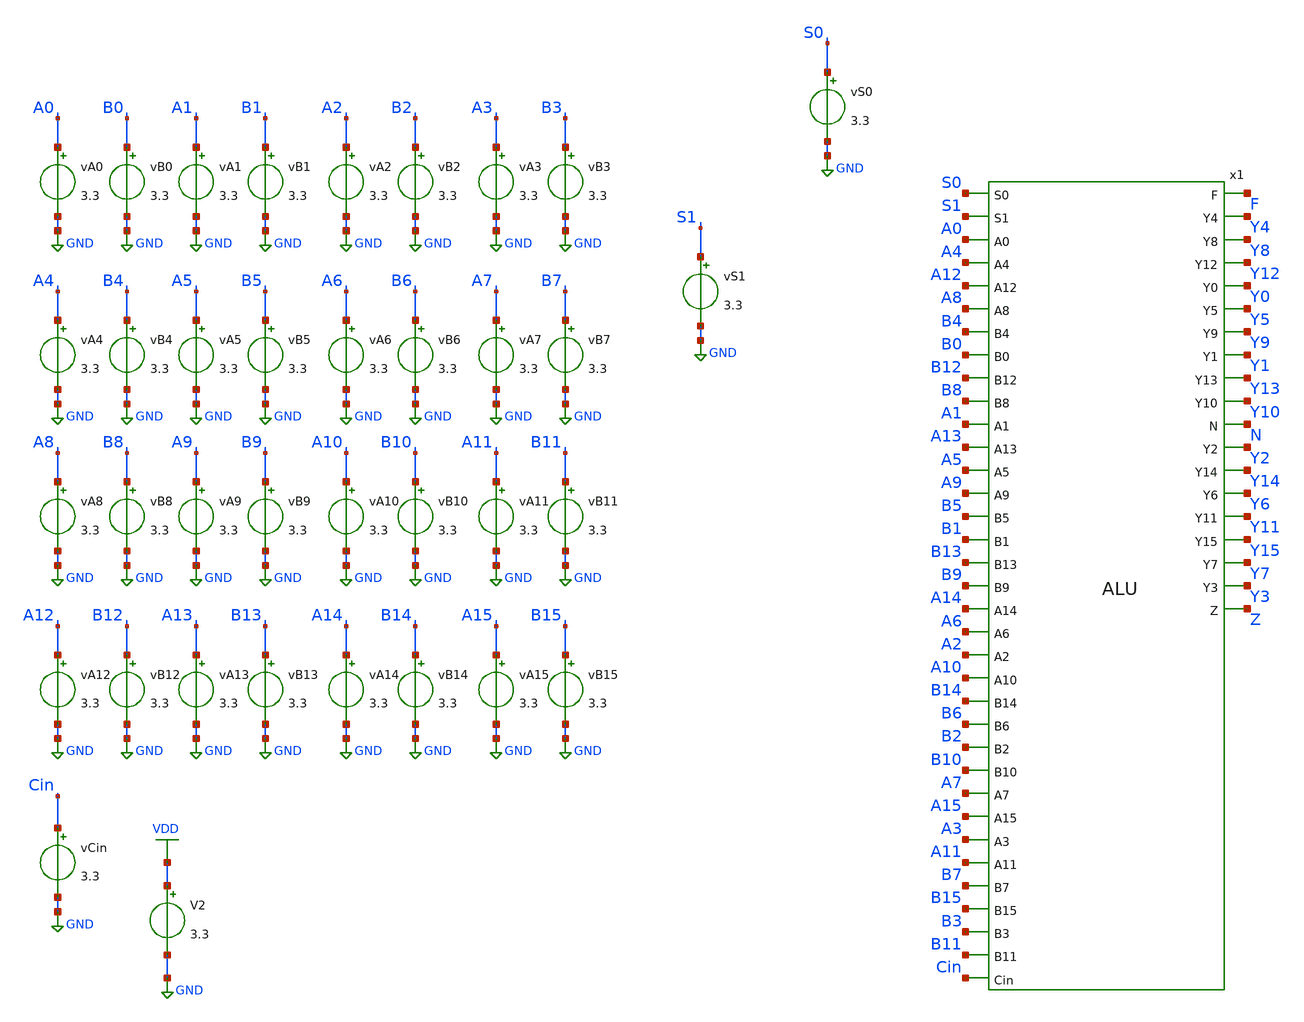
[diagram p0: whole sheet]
** sch_path: tbs/alu_tb_cmpless.sch
**.subckt alu_tb_cmpless
x1 S0 S1 F A0 A4 A12 A8 B4 B0 B12 B8 A1 A13 A5 A9 Y4 Y8 Y12 Y0 B5 B1 B13 B9 Y5 Y9 Y1 Y13 A14 A6 A2
+ A10 Y10 N Y2 Y14 Y6 B14 B6 B2 B10 Y11 Y15 Y7 Y3 A7 A15 A3 A11 B7 B15 B3 B11 Cin Z ALU
vA0 A0 GND 3.3
vB0 B0 GND 3.3
vA1 A1 GND 3.3
vB1 B1 GND 3.3
vA2 A2 GND 3.3
vB2 B2 GND 3.3
vA3 A3 GND 3.3
vB3 B3 GND 3.3
vA4 A4 GND 3.3
vB4 B4 GND 3.3
vA5 A5 GND 3.3
vB5 B5 GND 3.3
vA6 A6 GND 3.3
vB6 B6 GND 3.3
vA7 A7 GND 3.3
vB7 B7 GND 3.3
vA8 A8 GND 3.3
vB8 B8 GND 3.3
vA9 A9 GND 3.3
vB9 B9 GND 3.3
vA10 A10 GND 3.3
vB10 B10 GND 3.3
vA11 A11 GND 3.3
vB11 B11 GND 3.3
vA12 A12 GND 3.3
vB12 B12 GND 3.3
vA13 A13 GND 3.3
vB13 B13 GND 3.3
vA14 A14 GND 3.3
vB14 B14 GND 3.3
vA15 A15 GND 3.3
vB15 B15 GND 3.3
vS0 S0 GND 3.3
vS1 S1 GND 3.3
vCin Cin GND 3.3
V2 VDD GND 3.3
**** begin user architecture code


.control
  let vlow = 0
  let vhigh = 3.3

  * CMP via A + ~B + 1
  alter VS1 = $&vlow
  alter VS0 = $&vlow
  alter VCin = $&vhigh

  * A = 0x0003
  alter VA15 = $&vlow
  alter VA14 = $&vlow
  alter VA13 = $&vlow
  alter VA12 = $&vlow
  alter VA11 = $&vlow
  alter VA10 = $&vlow
  alter VA9  = $&vlow
  alter VA8  = $&vlow
  alter VA7  = $&vlow
  alter VA6  = $&vlow
  alter VA5  = $&vlow
  alter VA4  = $&vlow
  alter VA3  = $&vlow
  alter VA2  = $&vlow
  alter VA1  = $&vhigh
  alter VA0  = $&vhigh

  * B = ~0x0005 = 0xFFFA
  alter VB15 = $&vhigh
  alter VB14 = $&vhigh
  alter VB13 = $&vhigh
  alter VB12 = $&vhigh
  alter VB11 = $&vhigh
  alter VB10 = $&vhigh
  alter VB9  = $&vhigh
  alter VB8  = $&vhigh
  alter VB7  = $&vhigh
  alter VB6  = $&vhigh
  alter VB5  = $&vhigh
  alter VB4  = $&vhigh
  alter VB3  = $&vhigh
  alter VB2  = $&vlow
  alter VB1  = $&vhigh
  alter VB0  = $&vlow

  op
  echo EXPECTED: N=1, Z=0
  print v(n) v(z) v(f)

  tran 0.1n 30n
  meas tran vn find v(n) at=30n
  meas tran vz find v(z) at=30n
  meas tran vf find v(f) at=30n
  echo comparing two different numbers and z should not be raised and n should be raised
  print vn vz vf
  write alu_cmp_less_results.raw
.endc



.include $::180MCU_MODELS/design.ngspice
.lib $::180MCU_MODELS/sm141064.ngspice typical

**** end user architecture code
**.ends
.GLOBAL GND
.GLOBAL VDD
.end
